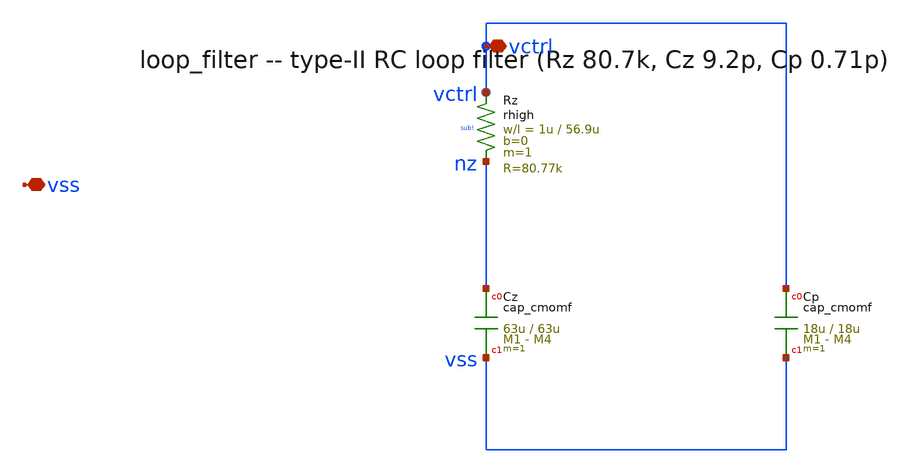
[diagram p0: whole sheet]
** sch_path: xschem/loop_filter.sch
**.subckt loop_filter vctrl vss
*.iopin vctrl
*.iopin vss
XRz vctrl nz sub! rhigh w=1u l=56.9u m=1 b=0 mm_ok=1
XCz nz vss cap_cmomf w=63u l=63u mmin=1 mmax=4 subblock=0 rfmodel=0 subscale=1 m=1 mm_ok=1
XCp vctrl vss cap_cmomf w=18u l=18u mmin=1 mmax=4 subblock=0 rfmodel=0 subscale=1 m=1 mm_ok=1
**.ends
.end
